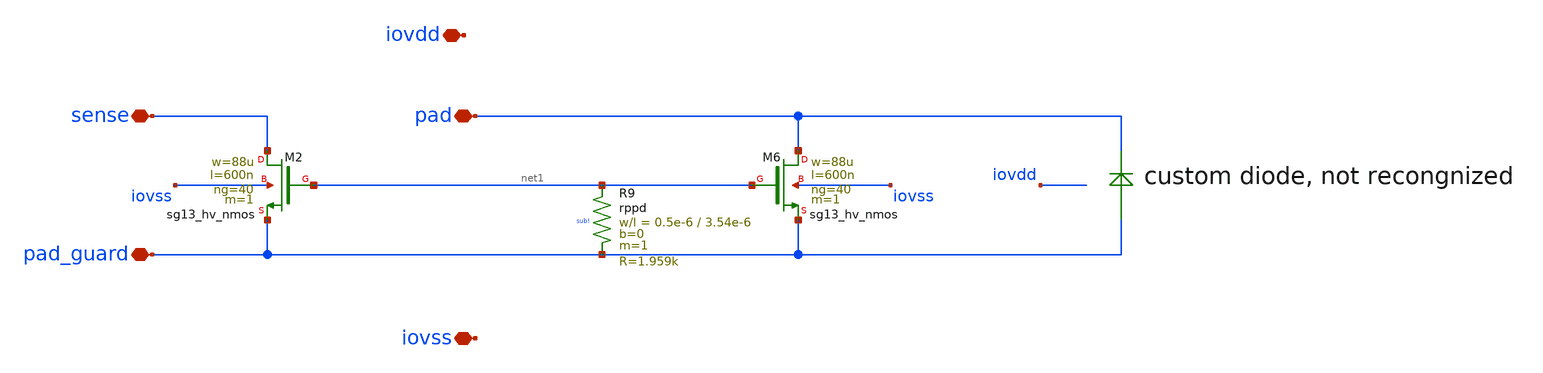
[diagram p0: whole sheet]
** sch_path: trident_test_structures/design_data/xschem/IOPadAnalogGuardLayerSense/pad_guard_to_vss_first_stage_esd_sense.sch
**.subckt pad_guard_to_vss_first_stage_esd_sense iovss pad_guard iovdd pad sense
*.iopin iovss
*.iopin pad_guard
*.iopin iovdd
*.iopin pad
*.iopin sense
XM6 pad net1 pad_guard iovss sg13_hv_nmos w=88u l=600n ng=40 m=1 mm_ok=1
XR9 net1 pad_guard sub! rppd w=0.5e-6 l=3.54e-6 m=1 b=0 mm_ok=1
XM2 sense net1 pad_guard iovss sg13_hv_nmos w=88u l=600n ng=40 m=1 mm_ok=1
**.ends
.end
